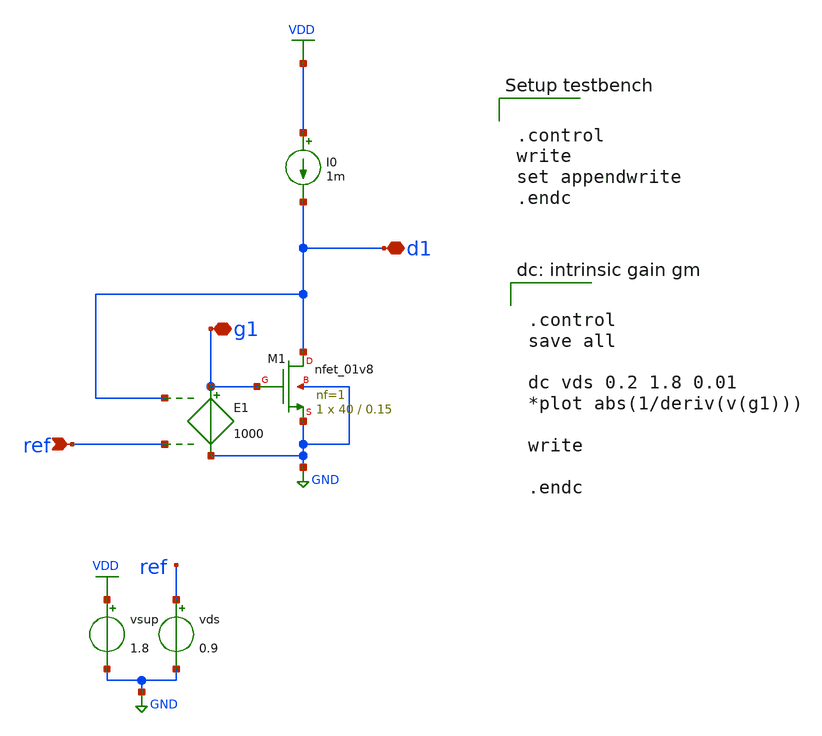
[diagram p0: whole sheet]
** sch_path: samples/sky130/nmos/test/nmos_intrinsic_gain.sch

*.lib $env(PDK_ROOT)/$env(PDK)/libs.tech/ngspice/sky130.lib.spice tt
.lib $env(PDK_ROOT)/$env(PDK)/libs.tech/ngspice/sky130.lib.spice.tt.red tt


.control
write
set appendwrite
.endc


**.subckt nmos_intrinsic_gain ref g1 d1
*.ipin ref
*.iopin g1
*.iopin d1
E1 g1 GND d1 ref 1000
I0 VDD d1 1m
XM1 d1 g1 GND GND sky130_fd_pr__nfet_01v8 L=0.15 W=40 nf=1 ad='int((nf+1)/2) * W/nf * 0.29' as='int((nf+2)/2) * W/nf * 0.29'
+ pd='2*int((nf+1)/2) * (W/nf + 0.29)' ps='2*int((nf+2)/2) * (W/nf + 0.29)' nrd='0.29 / W' nrs='0.29 / W'
+ sa=0 sb=0 sd=0 mult=1 m=1
vsup VDD GND 1.8
vds ref GND 0.9
**** begin user architecture code


.control
save all

dc vds 0.2 1.8 0.01
*plot abs(1/deriv(v(g1)))

write

.endc


**** end user architecture code
**.ends
.GLOBAL GND
.GLOBAL VDD
.end
